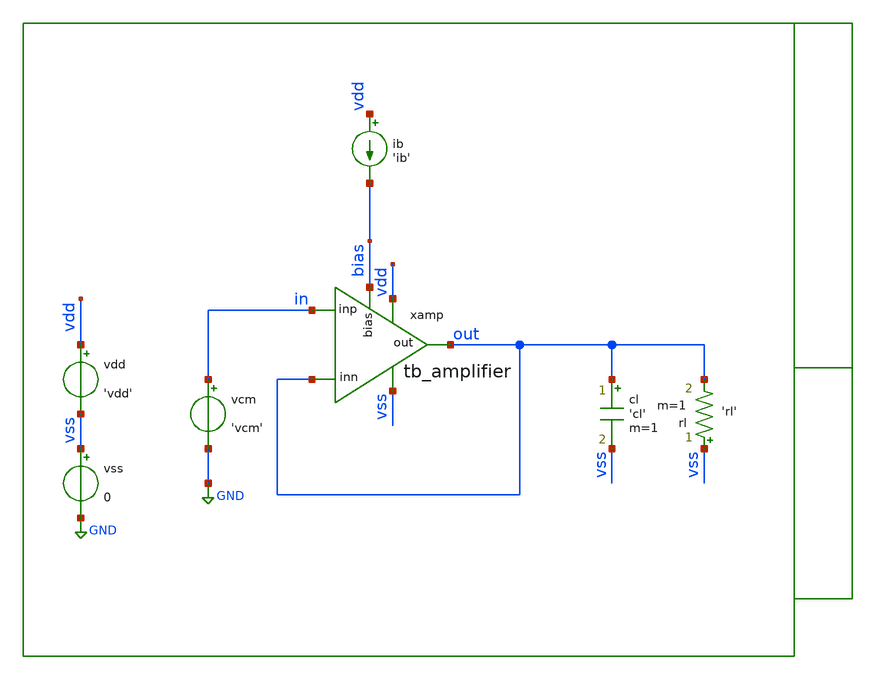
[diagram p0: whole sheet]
** sch_path: xschem/tb/testbuffer/tb_amplifier/mc_tb_amplifier.sch
**.subckt mc_tb_amplifier
ib vdd bias 'ib'
cl out vss 'cl' m=1
rl vss out 'rl' m=1
vcm in GND 'vcm'
vdd vdd vss 'vdd'
vss vss GND 0
xamp vdd out in out vss bias tb_amplifier
**** begin user architecture code


.param vdd=3.3
.param vcm='vdd/2'
.param ib=5.6u
.param cl=10p
.param rl=10e6


.control

let mc_runs   = 300
let seedvalue = 0
let steprun   = 0
let run       = 0

let vos_vec  = unitvec(mc_runs + 1)
let run_index = unitvec(mc_runs + 1)

dowhile run <= mc_runs

    alterparam sw_stat_global   = 1
    alterparam sw_stat_mismatch = 1
    reset

    save v(in) v(out)

    op

    let vos_vec[run] = v(out) - v(in)
    let run_index[run] = run

    let run = run + 1
end

setplot new
let vdiff = vos_vec
let vos = vdiff

print mean(vos)
print stddev(vos)

set wr_singlescale
set wr_vecnames
wrdata data.csv vos

.endc


 * Model Corners

.include $::CORNERS/ngspice/tt.spice
*.include $::CORNERS/ngspice/ff.spice
*.include $::CORNERS/ngspice/ss.spice
*.include $::CORNERS/ngspice/sf.spice
*.include $::CORNERS/ngspice/fs.spice

**** end user architecture code
**.ends

* expanding   symbol:  sch/testbuffer/tb_amplifier/tb_amplifier.sym # of pins=6
** sym_path: xschem/sch/testbuffer/tb_amplifier/tb_amplifier.sym
** sch_path: xschem/sch/testbuffer/tb_amplifier/tb_amplifier.sch
.subckt tb_amplifier vdd out inp inn vss bias
*.ipin inn
*.ipin inp
*.opin out
*.iopin bias
*.iopin vdd
*.iopin vss
XM3 mirr mirr vdd vdd pfet_06v0 L=4u W=16u nf=2 ad='int((nf+1)/2) * W/nf * 0.18u' as='int((nf+2)/2) * W/nf * 0.18u'
+ pd='2*int((nf+1)/2) * (W/nf + 0.18u)' ps='2*int((nf+2)/2) * (W/nf + 0.18u)' nrd='0.18u / W' nrs='0.18u / W'
+ sa=0 sb=0 sd=0 m=2 par=2
XM4 comp mirr vdd vdd pfet_06v0 L=4u W=16u nf=2 ad='int((nf+1)/2) * W/nf * 0.18u' as='int((nf+2)/2) * W/nf * 0.18u'
+ pd='2*int((nf+1)/2) * (W/nf + 0.18u)' ps='2*int((nf+2)/2) * (W/nf + 0.18u)' nrd='0.18u / W' nrs='0.18u / W'
+ sa=0 sb=0 sd=0 m=2 par=2
XM2 comp inp vcm vss nfet_06v0 L=2u W=16u nf=2 ad='int((nf+1)/2) * W/nf * 0.18u' as='int((nf+2)/2) * W/nf * 0.18u'
+ pd='2*int((nf+1)/2) * (W/nf + 0.18u)' ps='2*int((nf+2)/2) * (W/nf + 0.18u)' nrd='0.18u / W' nrs='0.18u / W'
+ sa=0 sb=0 sd=0 m=2 par=2
XM1 mirr inn vcm vss nfet_06v0 L=2u W=16u nf=2 ad='int((nf+1)/2) * W/nf * 0.18u' as='int((nf+2)/2) * W/nf * 0.18u'
+ pd='2*int((nf+1)/2) * (W/nf + 0.18u)' ps='2*int((nf+2)/2) * (W/nf + 0.18u)' nrd='0.18u / W' nrs='0.18u / W'
+ sa=0 sb=0 sd=0 m=2 par=2
XM5 vcm bias vss vss nfet_06v0 L=1u W=16u nf=2 ad='int((nf+1)/2) * W/nf * 0.18u' as='int((nf+2)/2) * W/nf * 0.18u'
+ pd='2*int((nf+1)/2) * (W/nf + 0.18u)' ps='2*int((nf+2)/2) * (W/nf + 0.18u)' nrd='0.18u / W' nrs='0.18u / W'
+ sa=0 sb=0 sd=0 m=2 par=2
XM6 out bias vss vss nfet_06v0 L=1u W=16u nf=2 ad='int((nf+1)/2) * W/nf * 0.18u' as='int((nf+2)/2) * W/nf * 0.18u'
+ pd='2*int((nf+1)/2) * (W/nf + 0.18u)' ps='2*int((nf+2)/2) * (W/nf + 0.18u)' nrd='0.18u / W' nrs='0.18u / W'
+ sa=0 sb=0 sd=0 m=12 par=12
XM7 out comp vdd vdd pfet_06v0 L=1u W=96u nf=12 ad='int((nf+1)/2) * W/nf * 0.18u' as='int((nf+2)/2) * W/nf * 0.18u'
+ pd='2*int((nf+1)/2) * (W/nf + 0.18u)' ps='2*int((nf+2)/2) * (W/nf + 0.18u)' nrd='0.18u / W' nrs='0.18u / W'
+ sa=0 sb=0 sd=0 m=1 par=1
XMB1 bias bias vss vss nfet_06v0 L=1u W=16u nf=2 ad='int((nf+1)/2) * W/nf * 0.18u' as='int((nf+2)/2) * W/nf * 0.18u'
+ pd='2*int((nf+1)/2) * (W/nf + 0.18u)' ps='2*int((nf+2)/2) * (W/nf + 0.18u)' nrd='0.18u / W' nrs='0.18u / W'
+ sa=0 sb=0 sd=0 m=2 par=2
XMB2 vbm bias vss vss nfet_06v0 L=1u W=16u nf=2 ad='int((nf+1)/2) * W/nf * 0.18u' as='int((nf+2)/2) * W/nf * 0.18u'
+ pd='2*int((nf+1)/2) * (W/nf + 0.18u)' ps='2*int((nf+2)/2) * (W/nf + 0.18u)' nrd='0.18u / W' nrs='0.18u / W'
+ sa=0 sb=0 sd=0 m=2 par=2
XMB3 vbm vbm vbt vdd pfet_06v0 L=1u W=16u nf=2 ad='int((nf+1)/2) * W/nf * 0.18u' as='int((nf+2)/2) * W/nf * 0.18u'
+ pd='2*int((nf+1)/2) * (W/nf + 0.18u)' ps='2*int((nf+2)/2) * (W/nf + 0.18u)' nrd='0.18u / W' nrs='0.18u / W'
+ sa=0 sb=0 sd=0 m=1 par=1
XMB4 vbt vbt vdd vdd pfet_06v0 L=1u W=16u nf=2 ad='int((nf+1)/2) * W/nf * 0.18u' as='int((nf+2)/2) * W/nf * 0.18u'
+ pd='2*int((nf+1)/2) * (W/nf + 0.18u)' ps='2*int((nf+2)/2) * (W/nf + 0.18u)' nrd='0.18u / W' nrs='0.18u / W'
+ sa=0 sb=0 sd=0 m=1 par=1
XRCC gc comp vdd ppolyf_u_1k_6p0 r_width=2e-6 r_length=38e-6 s=1 m=1
XMDUM1 vss vss vss vss nfet_06v0 L=2u W=16u nf=2 ad='int((nf+1)/2) * W/nf * 0.18u' as='int((nf+2)/2) * W/nf * 0.18u'
+ pd='2*int((nf+1)/2) * (W/nf + 0.18u)' ps='2*int((nf+2)/2) * (W/nf + 0.18u)' nrd='0.18u / W' nrs='0.18u / W'
+ sa=0 sb=0 sd=0 m=2 par=2
XMDUM2 vdd vdd vdd vdd pfet_06v0 L=4u W=16u nf=2 ad='int((nf+1)/2) * W/nf * 0.18u' as='int((nf+2)/2) * W/nf * 0.18u'
+ pd='2*int((nf+1)/2) * (W/nf + 0.18u)' ps='2*int((nf+2)/2) * (W/nf + 0.18u)' nrd='0.18u / W' nrs='0.18u / W'
+ sa=0 sb=0 sd=0 m=4 par=4
XC1 out gc cap_mim_2f0_m4m5_noshield c_width=30e-6 c_length=30e-6 m=1
.ends

.GLOBAL GND
.end
